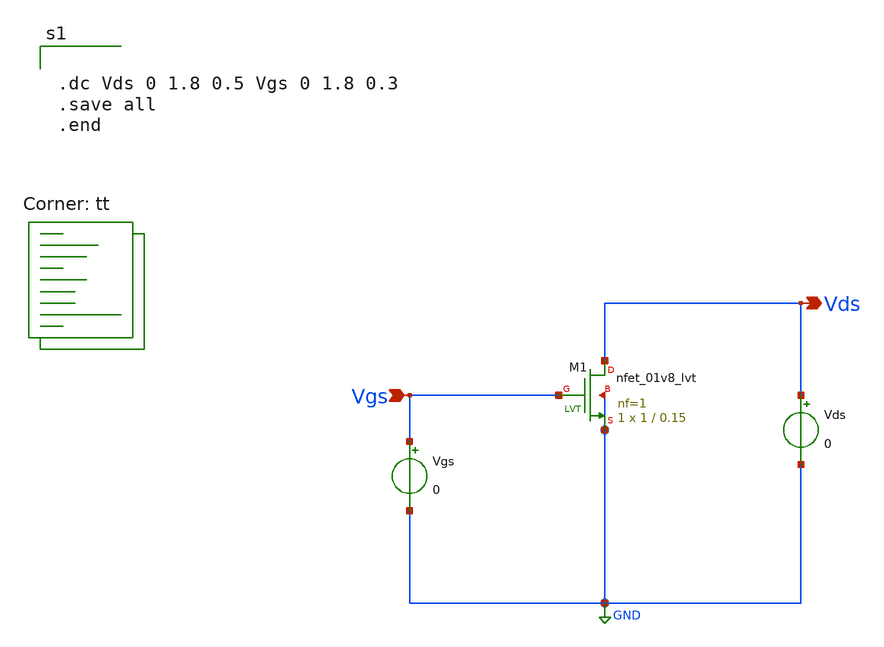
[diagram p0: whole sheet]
** sch_path: XSCHEM_DESIGNS/Nmos_Charactersitics.sch
**.subckt Nmos_Charactersitics Vgs Vds
*.ipin Vgs
*.opin Vds
XM1 Vds Vgs GND GND sky130_fd_pr__nfet_01v8_lvt L=0.15 W=1 nf=1 ad='int((1 + 1)/2) * 1 / 1 * 0.29' as='int((1 + 2)/2) * 1 / 1 * 0.29'
+ pd='2*int((1 + 1)/2) * (1 / 1 + 0.29)' ps='2*int((1 + 2)/2) * (1 / 1 + 0.29)' nrd='0.29 / 1 ' nrs='0.29 / 1 '
+ sa=0 sb=0 sd=0 mult=1 m=1
Vgs Vgs GND 0
Vds Vds GND 0
**** begin user architecture code
.lib $::SKYWATER_MODELS/sky130.lib.spice tt


.dc Vds 0 1.8 0.5 Vgs 0 1.8 0.3
.save all
.end


**** end user architecture code
**.ends
.GLOBAL GND
.end
